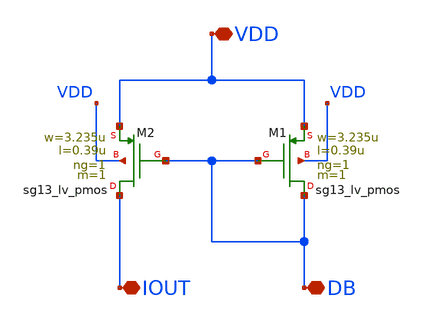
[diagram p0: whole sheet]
** sch_path: W2W-DAC/W2W_BOX/current_pmos.sch
**.subckt current_pmos VDD DB IOUT
*.iopin VDD
*.iopin DB
*.iopin IOUT
XM1 DB DB VDD VDD sg13_lv_pmos w=3.235u l=0.39u ng=1 m=1 mm_ok=1
XM2 IOUT DB VDD VDD sg13_lv_pmos w=3.235u l=0.39u ng=1 m=1 mm_ok=1
**.ends
.end
